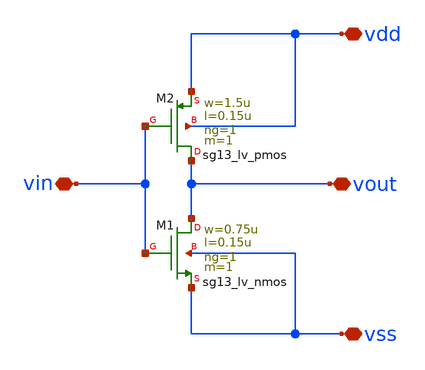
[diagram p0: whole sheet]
** sch_path: design/blocks/inverter/inverter.sch
**.subckt inverter vdd vout vss vin
*.iopin vdd
*.iopin vout
*.iopin vss
*.iopin vin
XM1 vout vin vss vss sg13_lv_nmos w=0.75u l=0.15u ng=1 m=1 mm_ok=1
XM2 vout vin vdd vdd sg13_lv_pmos w=1.5u l=0.15u ng=1 m=1 mm_ok=1
**.ends
.end
